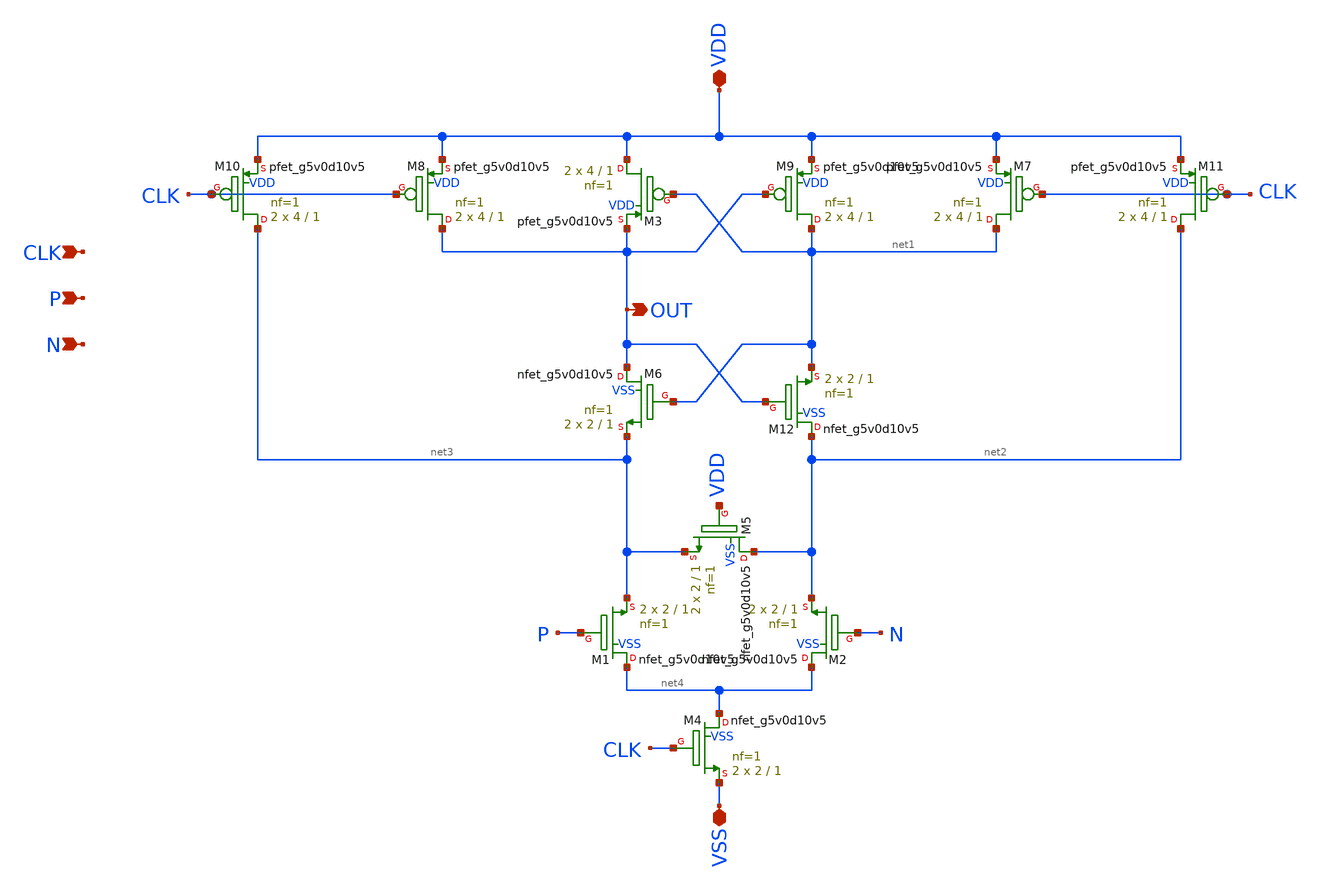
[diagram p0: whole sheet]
** sch_path: xschem/strongArmLatch.sch
**.subckt strongArmLatch VDD VSS P N CLK OUT
*.iopin VDD
*.iopin VSS
*.ipin P
*.ipin N
*.ipin CLK
*.opin OUT
XM1 net4 P net3 VSS sky130_fd_pr__nfet_g5v0d10v5 L=1 W=2 nf=1 ad='int((nf+1)/2) * W/nf * 0.29' as='int((nf+2)/2) * W/nf * 0.29'
+ pd='2*int((nf+1)/2) * (W/nf + 0.29)' ps='2*int((nf+2)/2) * (W/nf + 0.29)' nrd='0.29 / W' nrs='0.29 / W'
+ sa=0 sb=0 sd=0 mult=2 m=2
XM7 net1 CLK VDD VDD sky130_fd_pr__pfet_g5v0d10v5 L=1 W=4 nf=1 ad='int((nf+1)/2) * W/nf * 0.29' as='int((nf+2)/2) * W/nf * 0.29'
+ pd='2*int((nf+1)/2) * (W/nf + 0.29)' ps='2*int((nf+2)/2) * (W/nf + 0.29)' nrd='0.29 / W' nrs='0.29 / W'
+ sa=0 sb=0 sd=0 mult=2 m=2
XM8 OUT CLK VDD VDD sky130_fd_pr__pfet_g5v0d10v5 L=1 W=4 nf=1 ad='int((nf+1)/2) * W/nf * 0.29' as='int((nf+2)/2) * W/nf * 0.29'
+ pd='2*int((nf+1)/2) * (W/nf + 0.29)' ps='2*int((nf+2)/2) * (W/nf + 0.29)' nrd='0.29 / W' nrs='0.29 / W'
+ sa=0 sb=0 sd=0 mult=2 m=2
XM4 net4 CLK VSS VSS sky130_fd_pr__nfet_g5v0d10v5 L=1 W=2 nf=1 ad='int((nf+1)/2) * W/nf * 0.29' as='int((nf+2)/2) * W/nf * 0.29'
+ pd='2*int((nf+1)/2) * (W/nf + 0.29)' ps='2*int((nf+2)/2) * (W/nf + 0.29)' nrd='0.29 / W' nrs='0.29 / W'
+ sa=0 sb=0 sd=0 mult=2 m=2
XM5 net2 VDD net3 VSS sky130_fd_pr__nfet_g5v0d10v5 L=1 W=2 nf=1 ad='int((nf+1)/2) * W/nf * 0.29' as='int((nf+2)/2) * W/nf * 0.29'
+ pd='2*int((nf+1)/2) * (W/nf + 0.29)' ps='2*int((nf+2)/2) * (W/nf + 0.29)' nrd='0.29 / W' nrs='0.29 / W'
+ sa=0 sb=0 sd=0 mult=2 m=2
XM6 OUT net1 net3 VSS sky130_fd_pr__nfet_g5v0d10v5 L=1 W=2 nf=1 ad='int((nf+1)/2) * W/nf * 0.29' as='int((nf+2)/2) * W/nf * 0.29'
+ pd='2*int((nf+1)/2) * (W/nf + 0.29)' ps='2*int((nf+2)/2) * (W/nf + 0.29)' nrd='0.29 / W' nrs='0.29 / W'
+ sa=0 sb=0 sd=0 mult=2 m=2
XM2 net4 N net2 VSS sky130_fd_pr__nfet_g5v0d10v5 L=1 W=2 nf=1 ad='int((nf+1)/2) * W/nf * 0.29' as='int((nf+2)/2) * W/nf * 0.29'
+ pd='2*int((nf+1)/2) * (W/nf + 0.29)' ps='2*int((nf+2)/2) * (W/nf + 0.29)' nrd='0.29 / W' nrs='0.29 / W'
+ sa=0 sb=0 sd=0 mult=2 m=2
XM9 net1 OUT VDD VDD sky130_fd_pr__pfet_g5v0d10v5 L=1 W=4 nf=1 ad='int((nf+1)/2) * W/nf * 0.29' as='int((nf+2)/2) * W/nf * 0.29'
+ pd='2*int((nf+1)/2) * (W/nf + 0.29)' ps='2*int((nf+2)/2) * (W/nf + 0.29)' nrd='0.29 / W' nrs='0.29 / W'
+ sa=0 sb=0 sd=0 mult=2 m=2
XM3 VDD net1 OUT VDD sky130_fd_pr__pfet_g5v0d10v5 L=1 W=4 nf=1 ad='int((nf+1)/2) * W/nf * 0.29' as='int((nf+2)/2) * W/nf * 0.29'
+ pd='2*int((nf+1)/2) * (W/nf + 0.29)' ps='2*int((nf+2)/2) * (W/nf + 0.29)' nrd='0.29 / W' nrs='0.29 / W'
+ sa=0 sb=0 sd=0 mult=2 m=2
XM10 net3 CLK VDD VDD sky130_fd_pr__pfet_g5v0d10v5 L=1 W=4 nf=1 ad='int((nf+1)/2) * W/nf * 0.29' as='int((nf+2)/2) * W/nf * 0.29'
+ pd='2*int((nf+1)/2) * (W/nf + 0.29)' ps='2*int((nf+2)/2) * (W/nf + 0.29)' nrd='0.29 / W' nrs='0.29 / W'
+ sa=0 sb=0 sd=0 mult=2 m=2
XM11 net2 CLK VDD VDD sky130_fd_pr__pfet_g5v0d10v5 L=1 W=4 nf=1 ad='int((nf+1)/2) * W/nf * 0.29' as='int((nf+2)/2) * W/nf * 0.29'
+ pd='2*int((nf+1)/2) * (W/nf + 0.29)' ps='2*int((nf+2)/2) * (W/nf + 0.29)' nrd='0.29 / W' nrs='0.29 / W'
+ sa=0 sb=0 sd=0 mult=2 m=2
XM12 net2 OUT net1 VSS sky130_fd_pr__nfet_g5v0d10v5 L=1 W=2 nf=1 ad='int((nf+1)/2) * W/nf * 0.29' as='int((nf+2)/2) * W/nf * 0.29'
+ pd='2*int((nf+1)/2) * (W/nf + 0.29)' ps='2*int((nf+2)/2) * (W/nf + 0.29)' nrd='0.29 / W' nrs='0.29 / W'
+ sa=0 sb=0 sd=0 mult=2 m=2
**.ends
.end
